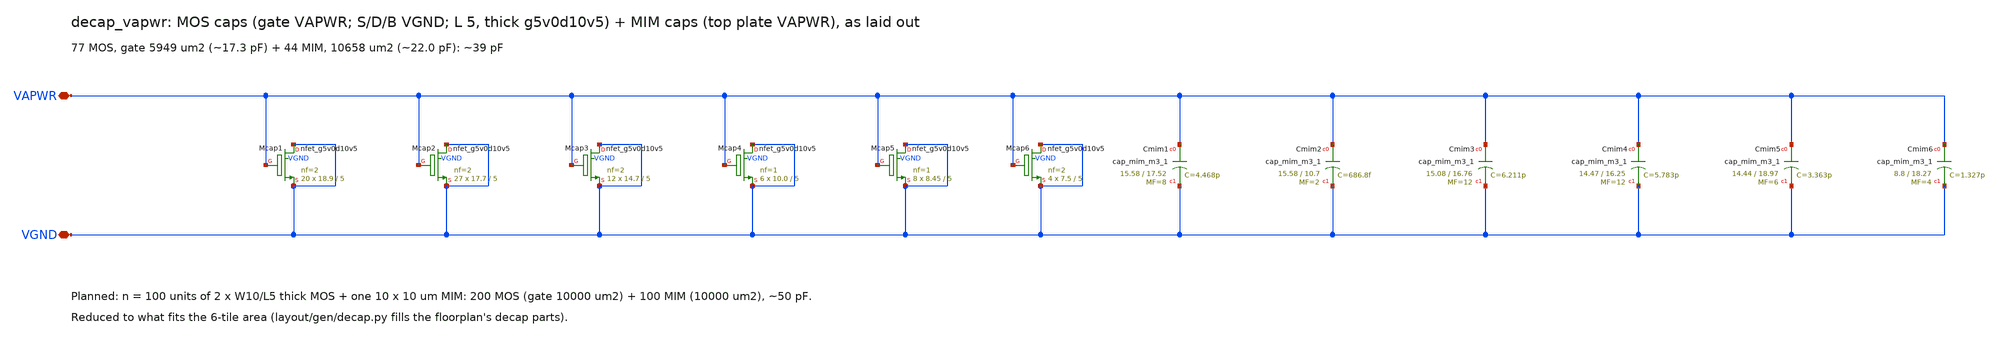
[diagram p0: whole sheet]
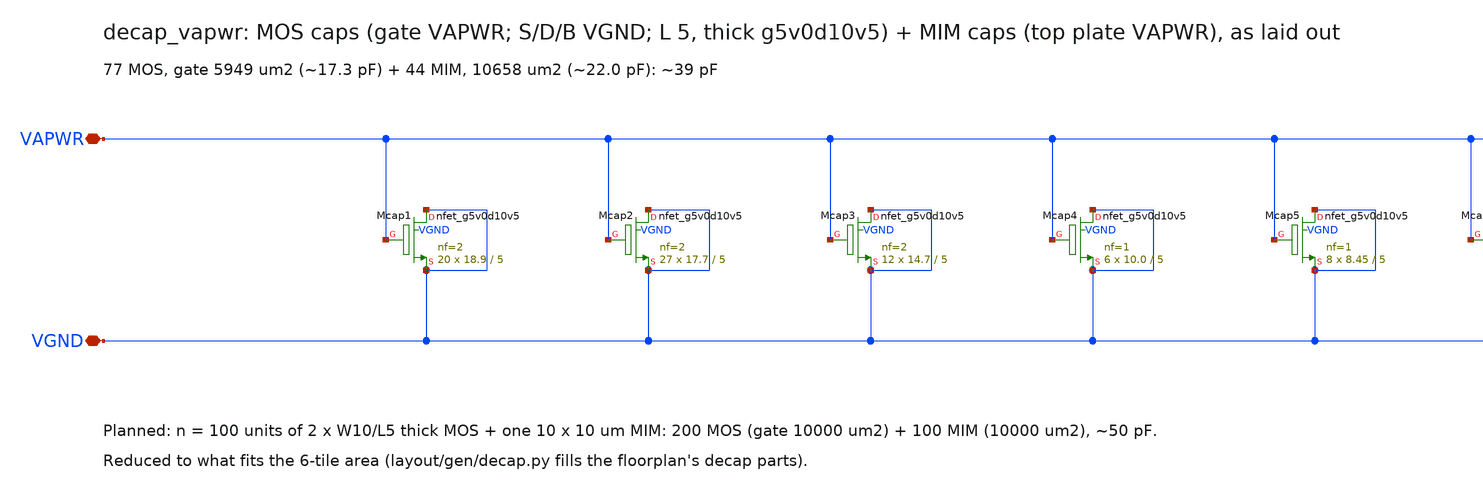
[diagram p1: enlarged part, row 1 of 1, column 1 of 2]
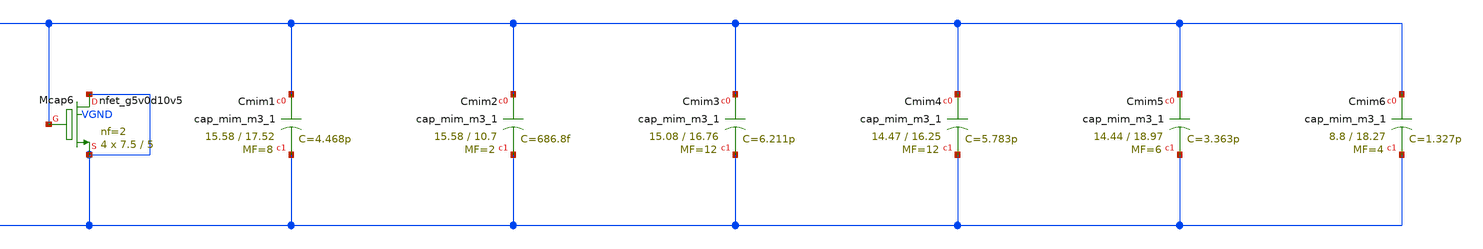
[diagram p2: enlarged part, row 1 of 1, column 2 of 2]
** sch_path: xschem/decap_vapwr.sch
**.subckt decap_vapwr VAPWR VGND
*.iopin VAPWR
*.iopin VGND
XMcap1 VGND VAPWR VGND VGND sky130_fd_pr__nfet_g5v0d10v5 L=5 W=18.9 nf=2 ad='int((nf+1)/2) * W/nf * 0.29'
+ as='int((nf+2)/2) * W/nf * 0.29' pd='2*int((nf+1)/2) * (W/nf + 0.29)' ps='2*int((nf+2)/2) * (W/nf + 0.29)'
+ nrd='0.29 / W' nrs='0.29 / W' sa=0 sb=0 sd=0 mult=20 m=20
XMcap2 VGND VAPWR VGND VGND sky130_fd_pr__nfet_g5v0d10v5 L=5 W=17.7 nf=2 ad='int((nf+1)/2) * W/nf * 0.29'
+ as='int((nf+2)/2) * W/nf * 0.29' pd='2*int((nf+1)/2) * (W/nf + 0.29)' ps='2*int((nf+2)/2) * (W/nf + 0.29)'
+ nrd='0.29 / W' nrs='0.29 / W' sa=0 sb=0 sd=0 mult=27 m=27
XMcap3 VGND VAPWR VGND VGND sky130_fd_pr__nfet_g5v0d10v5 L=5 W=14.7 nf=2 ad='int((nf+1)/2) * W/nf * 0.29'
+ as='int((nf+2)/2) * W/nf * 0.29' pd='2*int((nf+1)/2) * (W/nf + 0.29)' ps='2*int((nf+2)/2) * (W/nf + 0.29)'
+ nrd='0.29 / W' nrs='0.29 / W' sa=0 sb=0 sd=0 mult=12 m=12
XMcap4 VGND VAPWR VGND VGND sky130_fd_pr__nfet_g5v0d10v5 L=5 W=10.0 nf=1 ad='int((nf+1)/2) * W/nf * 0.29'
+ as='int((nf+2)/2) * W/nf * 0.29' pd='2*int((nf+1)/2) * (W/nf + 0.29)' ps='2*int((nf+2)/2) * (W/nf + 0.29)'
+ nrd='0.29 / W' nrs='0.29 / W' sa=0 sb=0 sd=0 mult=6 m=6
XMcap5 VGND VAPWR VGND VGND sky130_fd_pr__nfet_g5v0d10v5 L=5 W=8.45 nf=1 ad='int((nf+1)/2) * W/nf * 0.29'
+ as='int((nf+2)/2) * W/nf * 0.29' pd='2*int((nf+1)/2) * (W/nf + 0.29)' ps='2*int((nf+2)/2) * (W/nf + 0.29)'
+ nrd='0.29 / W' nrs='0.29 / W' sa=0 sb=0 sd=0 mult=8 m=8
XMcap6 VGND VAPWR VGND VGND sky130_fd_pr__nfet_g5v0d10v5 L=5 W=7.5 nf=2 ad='int((nf+1)/2) * W/nf * 0.29'
+ as='int((nf+2)/2) * W/nf * 0.29' pd='2*int((nf+1)/2) * (W/nf + 0.29)' ps='2*int((nf+2)/2) * (W/nf + 0.29)'
+ nrd='0.29 / W' nrs='0.29 / W' sa=0 sb=0 sd=0 mult=4 m=4
XCmim1 VAPWR VGND sky130_fd_pr__cap_mim_m3_1 W=15.58 L=17.52 MF=8 m=8
XCmim2 VAPWR VGND sky130_fd_pr__cap_mim_m3_1 W=15.58 L=10.7 MF=2 m=2
XCmim3 VAPWR VGND sky130_fd_pr__cap_mim_m3_1 W=15.08 L=16.76 MF=12 m=12
XCmim4 VAPWR VGND sky130_fd_pr__cap_mim_m3_1 W=14.47 L=16.25 MF=12 m=12
XCmim5 VAPWR VGND sky130_fd_pr__cap_mim_m3_1 W=14.44 L=18.97 MF=6 m=6
XCmim6 VAPWR VGND sky130_fd_pr__cap_mim_m3_1 W=8.8 L=18.27 MF=4 m=4
**.ends
.end
